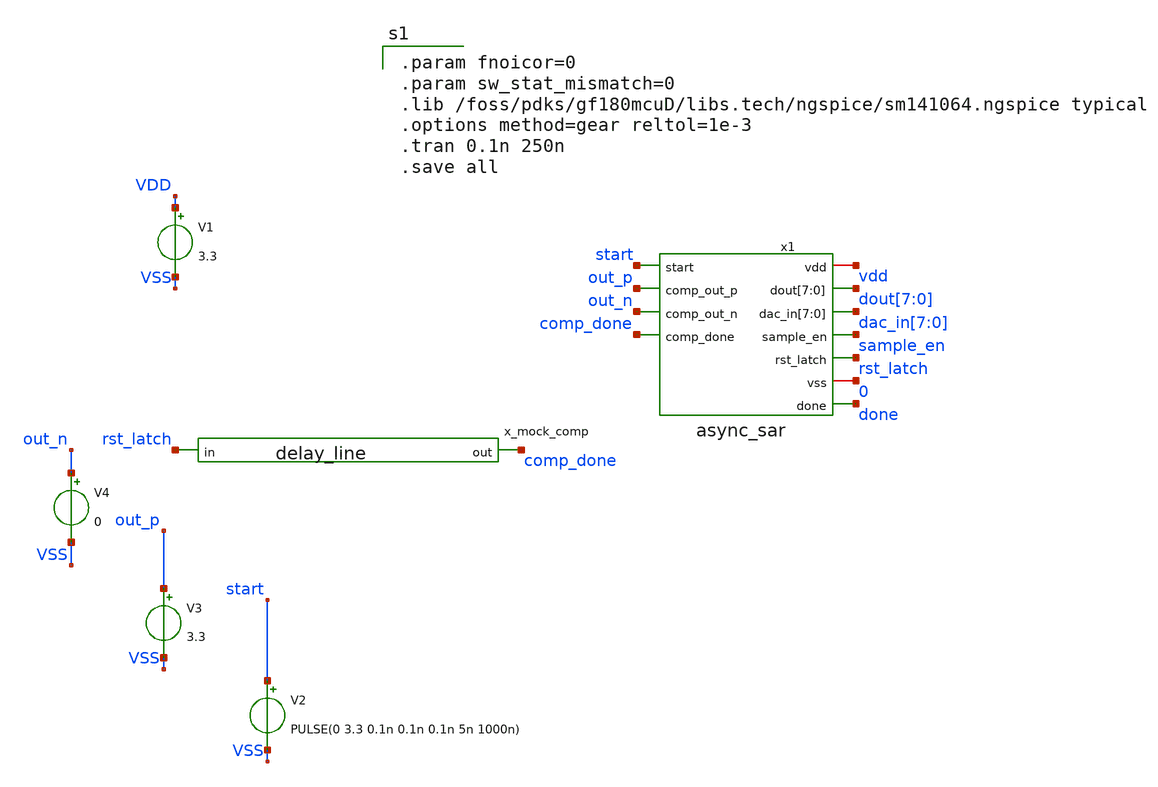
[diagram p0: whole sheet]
** sch_path: xschem/sar_adc/blocks/async_sar/testbench/tb_async_sar.sch
**.subckt tb_async_sar
V1 VDD VSS 3.3
V2 start VSS PULSE(0 3.3 0.1n 0.1n 0.1n 5n 1000n)
V3 out_p VSS 3.3
x_mock_comp comp_done rst_latch delay_line
x1 start out_p out_n comp_done vdd 0 sample_en rst_latch done dout[7] dout[6] dout[5] dout[4]
+ dout[3] dout[2] dout[1] dout[0] dac_in[7] dac_in[6] dac_in[5] dac_in[4] dac_in[3] dac_in[2] dac_in[1]
+ dac_in[0] async_sar
V4 out_n VSS 0
**** begin user architecture code

.param fnoicor=0
.param sw_stat_mismatch=0
.lib /foss/pdks/gf180mcuD/libs.tech/ngspice/sm141064.ngspice typical
.options method=gear reltol=1e-3
.tran 0.1n 250n
.save all

**** end user architecture code
**.ends
.end
